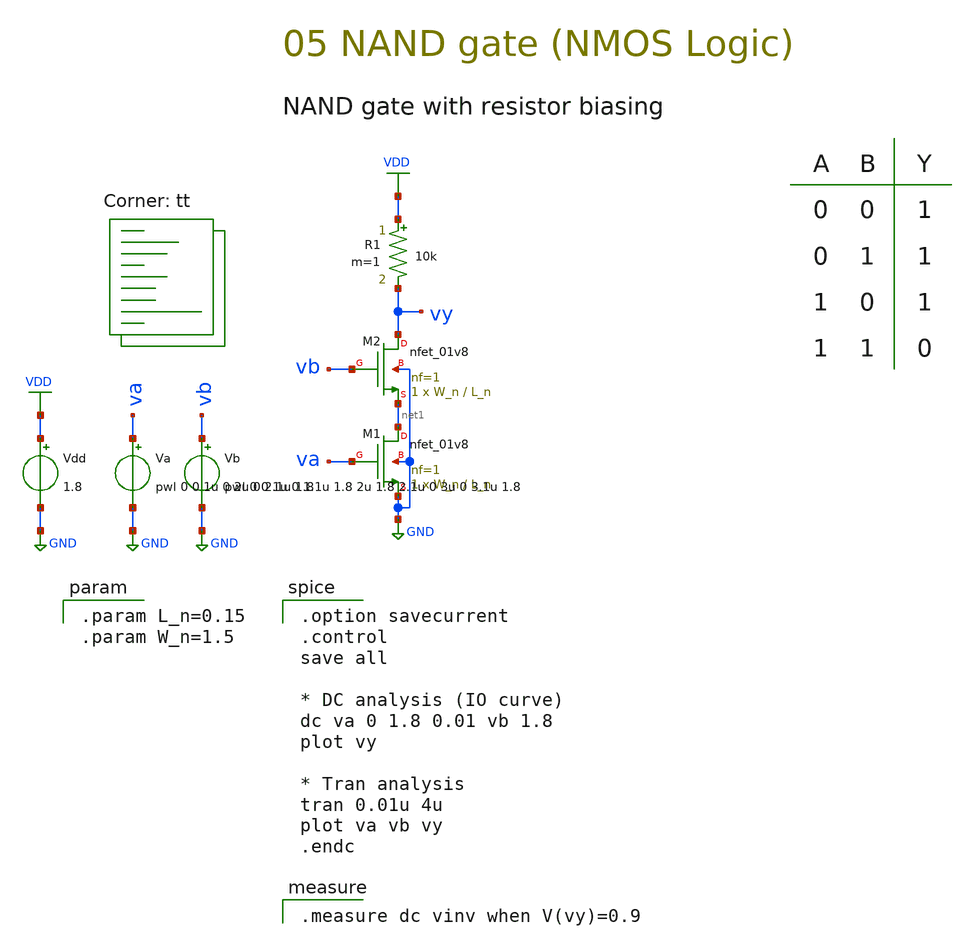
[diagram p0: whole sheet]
** sch_path: 05-a_NAND_R.sch
**.subckt 05-a_NAND_R
Vdd VDD GND 1.8
XM1 net1 va GND GND sky130_fd_pr__nfet_01v8 L=L_n W=W_n nf=1 ad='int((1 + 1)/2) * W_n / 1 * 0.29' as='int((1 + 2)/2) * W_n / 1 * 0.29'
+ pd='2*int((1 + 1)/2) * (W_n / 1 + 0.29)' ps='2*int((1 + 2)/2) * (W_n / 1 + 0.29)' nrd='0.29 / W_n ' nrs='0.29 / W_n '
+ sa=0 sb=0 sd=0 mult=1 m=1
XM2 vy vb net1 GND sky130_fd_pr__nfet_01v8 L=L_n W=W_n nf=1 ad='int((1 + 1)/2) * W_n / 1 * 0.29' as='int((1 + 2)/2) * W_n / 1 * 0.29'
+ pd='2*int((1 + 1)/2) * (W_n / 1 + 0.29)' ps='2*int((1 + 2)/2) * (W_n / 1 + 0.29)' nrd='0.29 / W_n ' nrs='0.29 / W_n '
+ sa=0 sb=0 sd=0 mult=1 m=1
Va va GND pwl 0 0 1u 0 2u 0 2.1u 1.8
R1 VDD vy 10k m=1
Vb vb GND pwl 0 0 1u 0 1.1u 1.8 2u 1.8 2.1u 0 3u 0 3.1u 1.8
**** begin user architecture code
.lib $::SKYWATER_MODELS/sky130.lib.spice tt

.param L_n=0.15
.param W_n=1.5


.option savecurrent
.control
save all

* DC analysis (IO curve)
dc va 0 1.8 0.01 vb 1.8
plot vy

* Tran analysis
tran 0.01u 4u
plot va vb vy
.endc


.measure dc vinv when V(vy)=0.9

**** end user architecture code
**.ends
.GLOBAL GND
.GLOBAL VDD
.end
